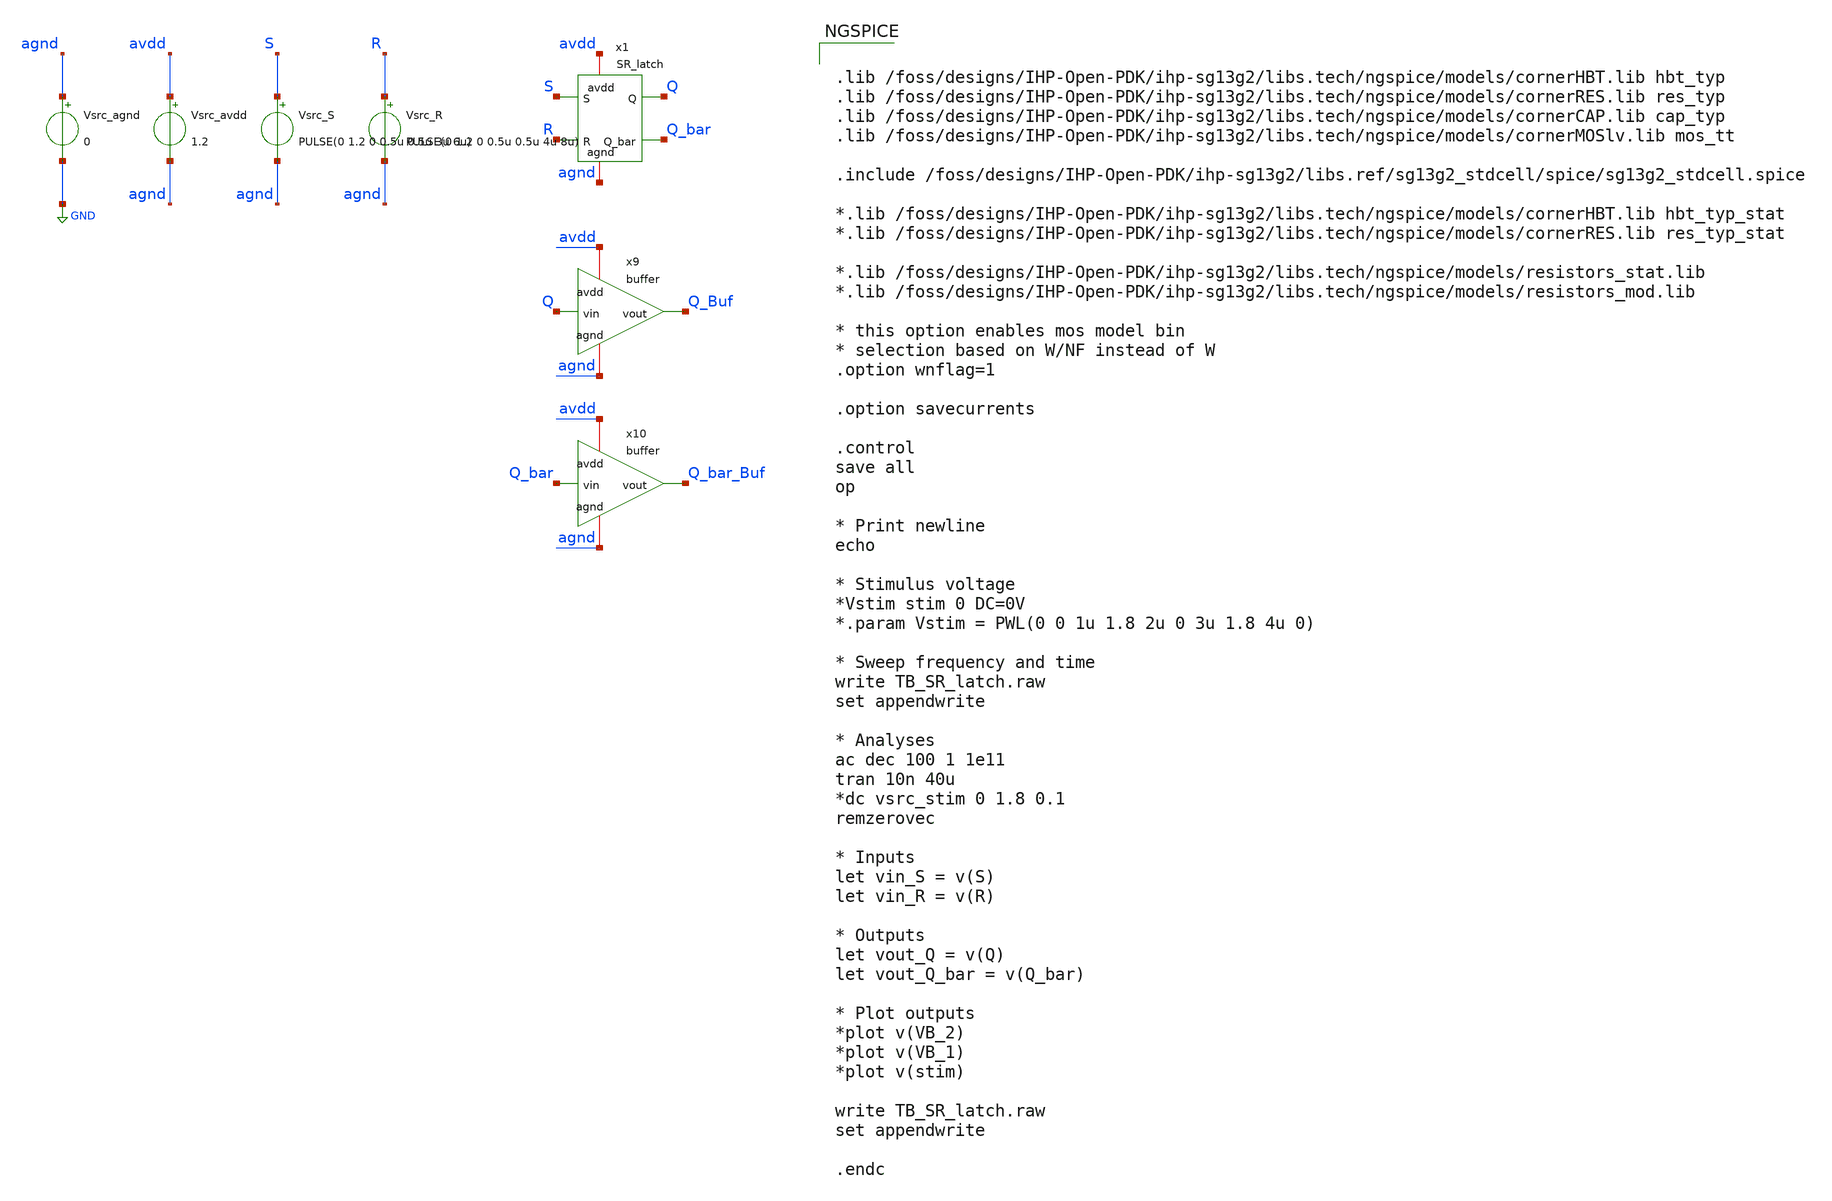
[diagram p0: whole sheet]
** sch_path: xschem/TB_SR_latch.sch
**.subckt TB_SR_latch
Vsrc_agnd agnd GND 0
Vsrc_avdd avdd agnd 1.2
Vsrc_S S agnd PULSE(0 1.2 0 0.5u 0.5u 3u 6u)
x1 avdd Q_bar Q agnd S R SR_latch
Vsrc_R R agnd PULSE(0 1.2 0 0.5u 0.5u 4u 8u)
x9 avdd Q Q_Buf agnd buffer
x10 avdd Q_bar Q_bar_Buf agnd buffer
**** begin user architecture code


.lib /foss/designs/IHP-Open-PDK/ihp-sg13g2/libs.tech/ngspice/models/cornerHBT.lib hbt_typ
.lib /foss/designs/IHP-Open-PDK/ihp-sg13g2/libs.tech/ngspice/models/cornerRES.lib res_typ
.lib /foss/designs/IHP-Open-PDK/ihp-sg13g2/libs.tech/ngspice/models/cornerCAP.lib cap_typ
.lib /foss/designs/IHP-Open-PDK/ihp-sg13g2/libs.tech/ngspice/models/cornerMOSlv.lib mos_tt

.include /foss/designs/IHP-Open-PDK/ihp-sg13g2/libs.ref/sg13g2_stdcell/spice/sg13g2_stdcell.spice

*.lib /foss/designs/IHP-Open-PDK/ihp-sg13g2/libs.tech/ngspice/models/cornerHBT.lib hbt_typ_stat
*.lib /foss/designs/IHP-Open-PDK/ihp-sg13g2/libs.tech/ngspice/models/cornerRES.lib res_typ_stat

*.lib /foss/designs/IHP-Open-PDK/ihp-sg13g2/libs.tech/ngspice/models/resistors_stat.lib
*.lib /foss/designs/IHP-Open-PDK/ihp-sg13g2/libs.tech/ngspice/models/resistors_mod.lib

* this option enables mos model bin
* selection based on W/NF instead of W
.option wnflag=1

.option savecurrents

.control
save all
op

* Print newline
echo

* Stimulus voltage
*Vstim stim 0 DC=0V
*.param Vstim = PWL(0 0 1u 1.8 2u 0 3u 1.8 4u 0)

* Sweep frequency and time
write TB_SR_latch.raw
set appendwrite

* Analyses
ac dec 100 1 1e11
tran 10n 40u
*dc vsrc_stim 0 1.8 0.1
remzerovec

* Inputs
let vin_S = v(S)
let vin_R = v(R)

* Outputs
let vout_Q = v(Q)
let vout_Q_bar = v(Q_bar)

* Plot outputs
*plot v(VB_2)
*plot v(VB_1)
*plot v(stim)

write TB_SR_latch.raw
set appendwrite

.endc


**** end user architecture code
**.ends

* expanding   symbol:  SR_latch.sym # of pins=6
** sym_path: xschem/SR_latch.sym
** sch_path: xschem/SR_latch.sch
.subckt SR_latch avdd Q_bar Q agnd S R
*.ipin R
*.opin Q_bar
*.ipin S
*.opin Q
*.iopin avdd
*.iopin agnd
XQ2 Q_bar net2 agnd agnd npn13G2 Nx=1 mm_ok=1
XQ1 Q net1 agnd agnd npn13G2 Nx=1 mm_ok=1
XR3 net1 R sub! rppd w=0.5e-6 l=20e-6 m=1 b=0 mm_ok=1
XR1 S net2 sub! rppd w=0.5e-6 l=20e-6 m=1 b=0 mm_ok=1
XR2 net1 agnd sub! rhigh w=0.5e-6 l=20e-6 m=1 b=0 mm_ok=1
XR4 net2 agnd sub! rhigh w=0.5e-6 l=20e-6 m=1 b=0 mm_ok=1
XR5 net2 Q sub! rppd w=0.5e-6 l=20e-6 m=1 b=0 mm_ok=1
XR6 Q_bar net1 sub! rppd w=0.5e-6 l=20e-6 m=1 b=0 mm_ok=1
XR7 avdd Q sub! rppd w=0.5e-6 l=2e-6 m=1 b=0 mm_ok=1
XR8 avdd Q_bar sub! rppd w=0.5e-6 l=2e-6 m=1 b=0 mm_ok=1
.ends


* expanding   symbol:  buffer.sym # of pins=4
** sym_path: xschem/buffer.sym
** sch_path: xschem/buffer.sch
.subckt buffer avdd vin vout agnd
*.iopin avdd
*.ipin vin
*.opin vout
*.iopin agnd
x1 avdd vin net1 agnd inverter
x2 avdd net1 vout agnd inverter
.ends


* expanding   symbol:  inverter.sym # of pins=4
** sym_path: xschem/inverter.sym
** sch_path: xschem/inverter.sch
.subckt inverter avdd vin vout agnd
*.iopin avdd
*.ipin vin
*.opin vout
*.iopin agnd
XQ1 vout base agnd agnd npn13G2 Nx=10 mm_ok=1
XR1 avdd vout sub! rhigh w=1e-6 l=0.5e-6 m=1 b=0 mm_ok=1
XR2 base vin sub! rhigh w=0.5e-6 l=0.5e-6 m=1 b=0 mm_ok=1
.ends

.GLOBAL GND
.end
